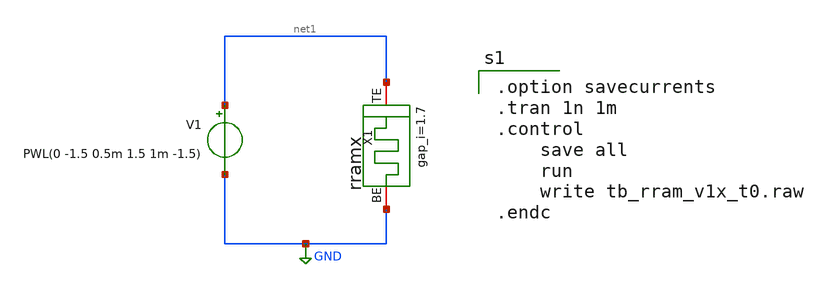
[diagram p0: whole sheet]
** sch_path: designs/tb_memristor/tb_rram_v1x_t0.sch
**.subckt tb_rram_v1x_t0
V1 net1 GND PWL(0 -1.5 0.5m 1.5 1m -1.5)
.save i(v1)
X1 net1 GND rram_cell gap_i=1.7
**** begin user architecture code

.option savecurrents
.tran 1n 1m
.control
	save all
	run
	write tb_rram_v1x_t0.raw
.endc


.subckt rram_cell BE TE gap_i=0.1
N1 BE TE rram_model
.model rram_model rram gap_initial={gap_i}
.ends rram_cell

.control
pre_osdi /foss/designs/spike_130/designs/memristors/rram_v1/rram.osdi
.endc

**** end user architecture code
**.ends
.GLOBAL GND
.end
